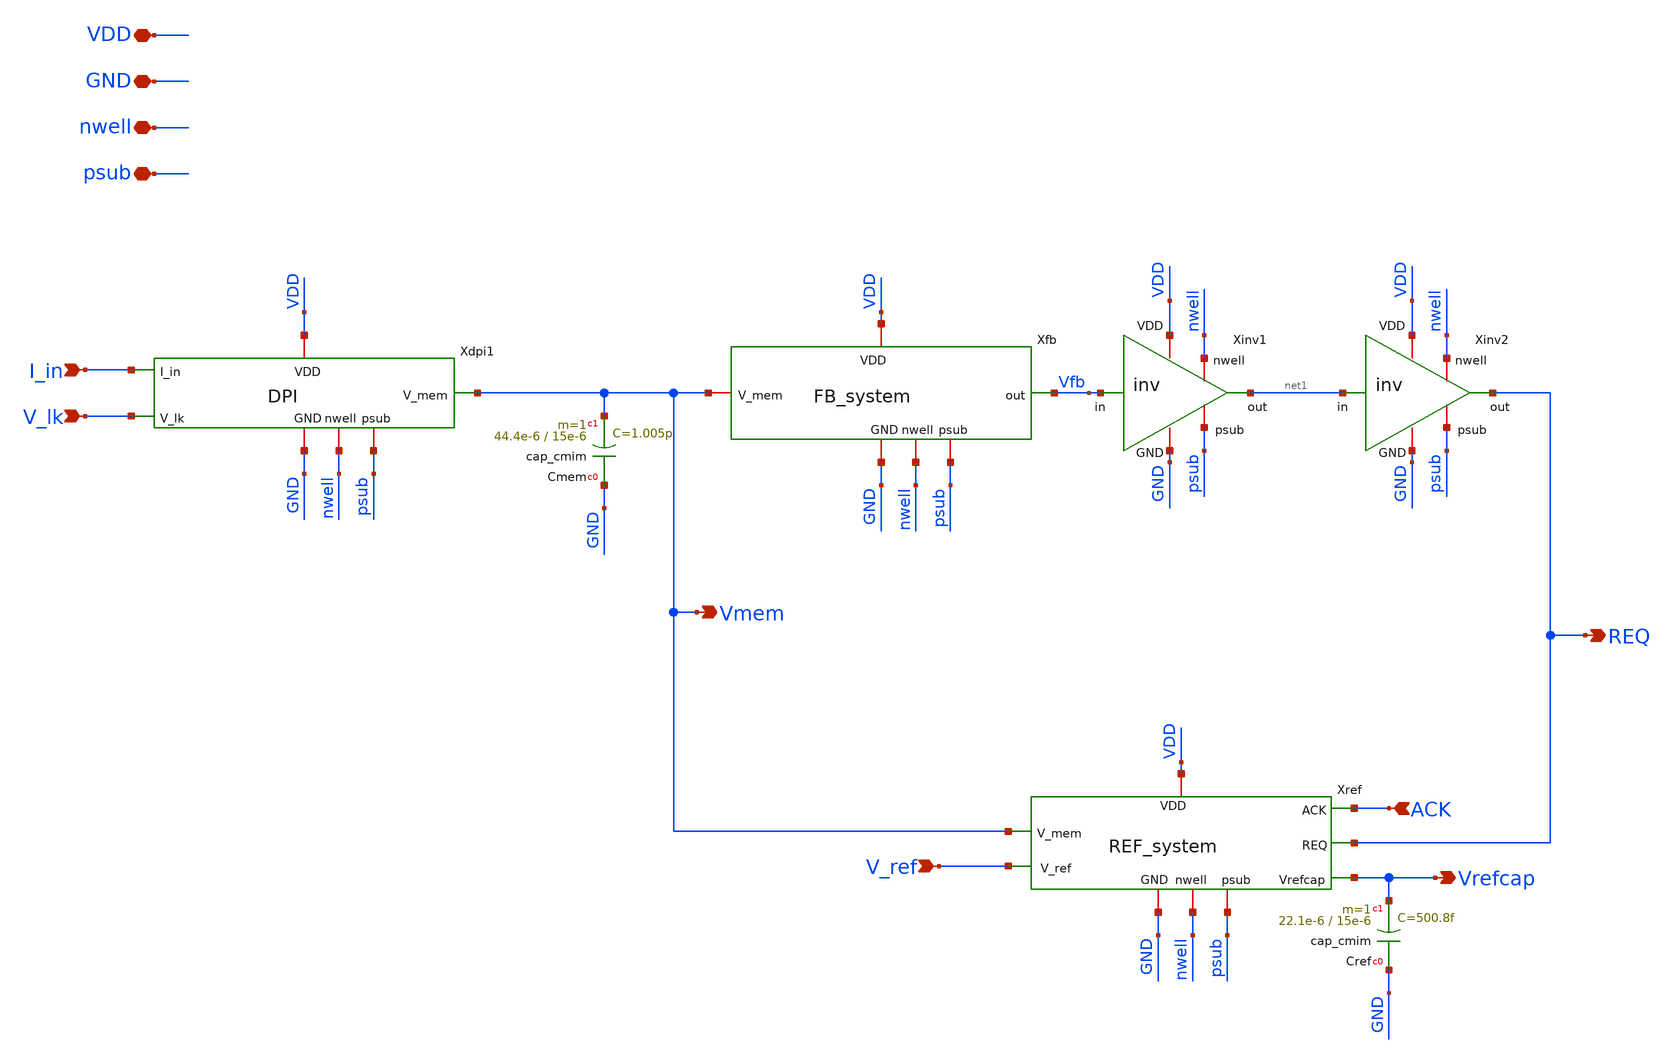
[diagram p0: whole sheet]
** sch_path: xschem/neuron_noahp.sch
**.subckt neuron_noahp V_ref GND VDD REQ ACK I_in V_lk Vmem Vrefcap psub nwell
*.ipin V_ref
*.iopin GND
*.iopin VDD
*.opin REQ
*.ipin ACK
*.ipin I_in
*.ipin V_lk
*.opin Vmem
*.opin Vrefcap
*.iopin psub
*.iopin nwell
Xinv1 VDD nwell net1 Vfb psub GND inv
Xinv2 VDD nwell REQ net1 psub GND inv
Xdpi1 I_in VDD Vmem V_lk GND nwell psub DPI
Xfb VDD Vfb Vmem GND nwell psub FB_system
Xref ACK Vmem REQ Vrefcap GND V_ref VDD nwell psub REF_system
XCmem GND Vmem cap_cmim w=44.4e-6 l=15e-6 m=1 mm_ok=1
XCref GND Vrefcap cap_cmim w=22.1e-6 l=15e-6 m=1 mm_ok=1
**.ends

* expanding   symbol:  inv.sym # of pins=6
** sym_path: xschem/inv.sym
** sch_path: xschem/inv.sch
.subckt inv VDD nwell out in psub GND
*.ipin in
*.iopin GND
*.opin out
*.iopin VDD
*.iopin nwell
*.iopin psub
XM1 out in VDD nwell sg13_hv_pmos w=4u l=0.5u ng=1 m=1 mm_ok=1
XM2 out in GND psub sg13_hv_nmos w=4u l=0.5u ng=1 m=1 mm_ok=1
XR1 GND psub ptap1 R=122.5 w=2e-6 l=1e-6
XR2 VDD nwell ntap1 R=122.5 w=2e-6 l=1e-6
.ends


* expanding   symbol:  DPI.sym # of pins=7
** sym_path: xschem/DPI.sym
** sch_path: xschem/DPI.sch
.subckt DPI I_in VDD V_mem V_lk GND nwell psub
*.opin V_mem
*.ipin V_lk
*.ipin I_in
*.iopin VDD
*.iopin GND
*.iopin nwell
*.iopin psub
XMdifl GND V_lk I_in nwell sg13_hv_pmos w=2u l=2u ng=2 m=8 mm_ok=1
XMdifr V_mem V_mem I_in nwell sg13_hv_pmos w=2u l=2u ng=2 m=8 mm_ok=1
XMtau V_mem V_lk GND psub sg13_hv_nmos w=4u l=4u ng=2 m=4 mm_ok=1
XR1 VDD nwell ntap1 R=16.73 w=25.2e-6 l=0.3e-6
XR2 VDD nwell ntap1 R=46.01 w=0.3e-6 l=9e-6
XR3 VDD nwell ntap1 R=46.01 w=0.3e-6 l=9e-6
XR4 GND psub ptap1 R=3.342 w=25.7e-6 l=9e-6 rw=0.3e-6
XMdum1 VDD VDD VDD nwell sg13_hv_pmos w=5u l=2u ng=10 m=2 mm_ok=1
XMdum2 I_in VDD VDD nwell sg13_hv_pmos w=1u l=2u ng=1 m=8 mm_ok=1
XMdum3 GND GND GND psub sg13_hv_nmos w=2u l=4u ng=4 m=2 mm_ok=1
XMdum4 GND GND GND psub sg13_hv_nmos w=0.5u l=3u ng=1 m=4 mm_ok=1
XMdum5 GND GND GND psub sg13_hv_nmos w=2u l=3u ng=1 m=4 mm_ok=1
.ends


* expanding   symbol:  FB_system.sym # of pins=6
** sym_path: xschem/FB_system.sym
** sch_path: xschem/FB_system.sch
.subckt FB_system VDD out V_mem GND nwell psub
*.opin out
*.iopin V_mem
*.iopin VDD
*.iopin GND
*.iopin nwell
*.iopin psub
XMmirr Vmir Vmir VDD nwell sg13_hv_pmos w=4u l=2u ng=4 m=1 mm_ok=1
XMmirl4 V_mem Vmir net1 nwell sg13_hv_pmos w=1u l=2u ng=1 m=1 mm_ok=1
XMthr out V_mem Vmir nwell sg13_hv_pmos w=4u l=2u ng=4 m=1 mm_ok=1
XMmem1 out V_mem net2 psub sg13_hv_nmos w=1u l=2u ng=1 m=2 mm_ok=1
XMmirl3 net1 Vmir net3 nwell sg13_hv_pmos w=1u l=2u ng=1 m=1 mm_ok=1
XMmirl2 net3 Vmir net4 nwell sg13_hv_pmos w=1u l=2u ng=1 m=1 mm_ok=1
XMmirl1 net4 Vmir VDD nwell sg13_hv_pmos w=1u l=2u ng=1 m=1 mm_ok=1
XMmem2 net2 V_mem net5 psub sg13_hv_nmos w=1u l=2u ng=1 m=2 mm_ok=1
XMmem3 net5 V_mem net6 psub sg13_hv_nmos w=1u l=2u ng=1 m=2 mm_ok=1
XMmem4 net6 V_mem GND psub sg13_hv_nmos w=1u l=2u ng=1 m=2 mm_ok=1
XMdum1 GND GND GND psub sg13_hv_nmos w=6u l=2u ng=6 m=2 mm_ok=1
XMdum2 GND GND GND psub sg13_hv_nmos w=1u l=2u ng=1 m=2 mm_ok=1
XMdum3 out GND GND psub sg13_hv_nmos w=1u l=2u ng=1 m=2 mm_ok=1
XMdum4 VDD VDD VDD nwell sg13_hv_pmos w=6u l=2u ng=6 m=2 mm_ok=1
XMdum5 VDD VDD VDD nwell sg13_hv_pmos w=1u l=2u ng=1 m=3 mm_ok=1
XMdum6 out VDD VDD nwell sg13_hv_pmos w=1u l=2u ng=1 m=2 mm_ok=1
XMdum7 V_mem VDD VDD nwell sg13_hv_pmos w=1u l=2u ng=1 m=1 mm_ok=1
.ends


* expanding   symbol:  REF_system.sym # of pins=9
** sym_path: xschem/REF_system.sym
** sch_path: xschem/REF_system.sch
.subckt REF_system ACK V_mem REQ Vrefcap GND V_ref VDD nwell psub
*.iopin VDD
*.iopin GND
*.ipin V_ref
*.ipin REQ
*.ipin ACK
*.ipin V_mem
*.opin Vrefcap
*.iopin psub
*.iopin nwell
XM10 Vrefcap REQ net2 nwell sg13_hv_pmos w=1u l=0.5u ng=1 m=1 mm_ok=1
XM11 Vrefcap REQ net1 psub sg13_hv_nmos w=1u l=0.5u ng=1 m=1 mm_ok=1
XM12 net2 ACK VDD nwell sg13_hv_pmos w=1u l=0.5u ng=1 m=1 mm_ok=1
XM13 V_mem Vrefcap GND psub sg13_hv_nmos w=1u l=0.5u ng=1 m=1 mm_ok=1
XM14 net1 V_ref GND psub sg13_hv_nmos w=4u l=4u ng=2 m=4 mm_ok=1
XMdum3 GND GND GND psub sg13_hv_nmos w=2u l=4u ng=4 m=2 mm_ok=1
XMdum4 GND GND GND psub sg13_hv_nmos w=0.5u l=3u ng=1 m=4 mm_ok=1
XMdum5 GND GND GND psub sg13_hv_nmos w=2u l=3u ng=1 m=4 mm_ok=1
XR4 GND psub ptap1 R=3.342 w=25.7e-6 l=9e-6 rw=0.3e-6
XR1 VDD nwell ntap1 R=3.748 w=24e-6 l=7e-6 rw=0.3e-6
.ends

.end
